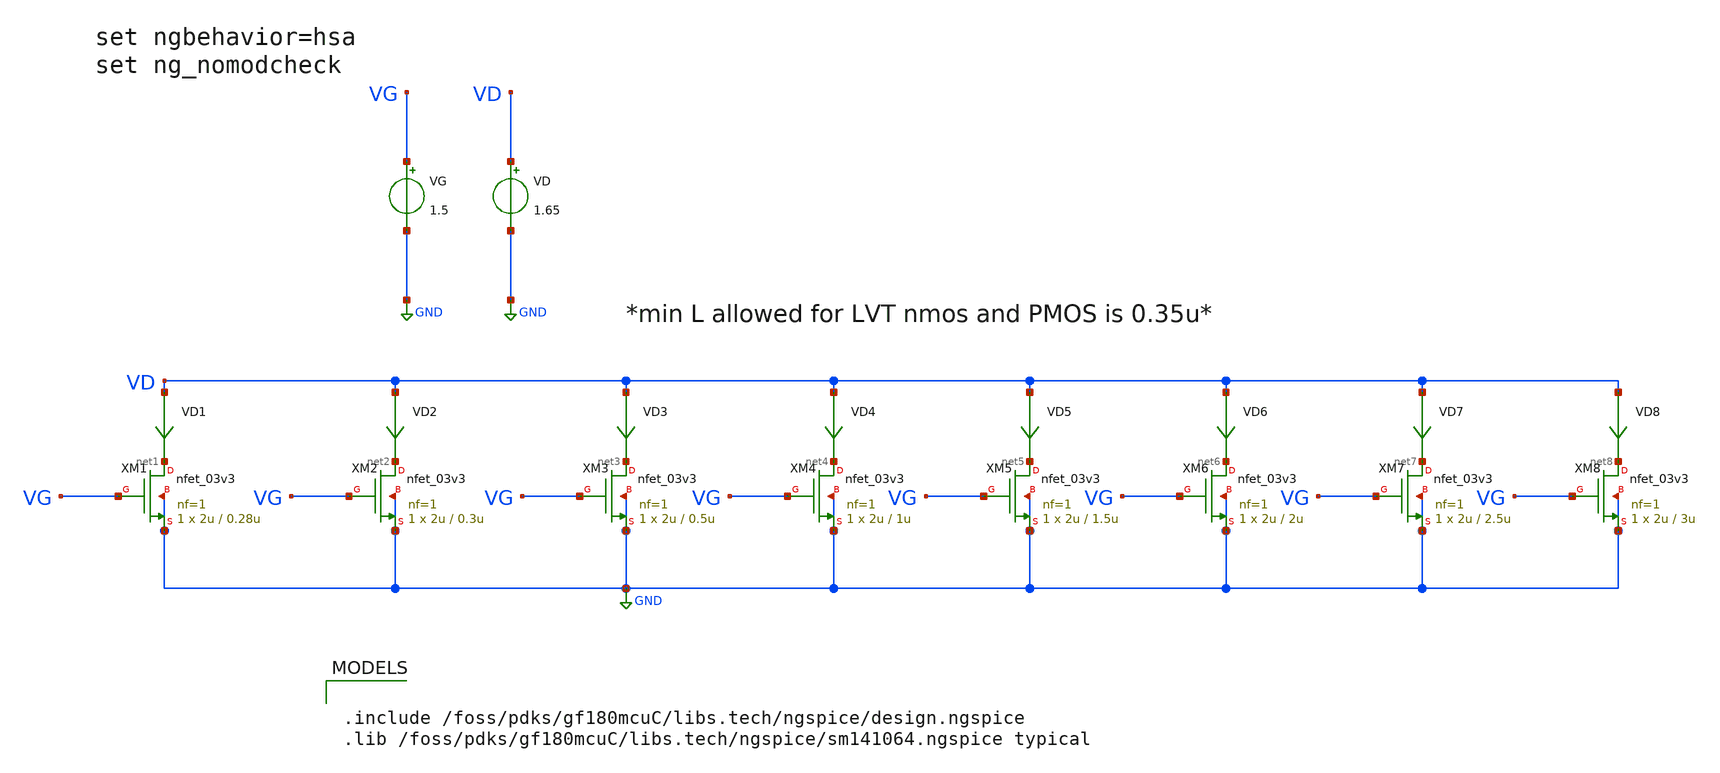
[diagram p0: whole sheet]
** sch_path: Testbench/gmid_nmos_nfet_03v3_tb.sch
**.subckt gmid_nmos_nfet_03v3_tb
VG VG GND 1.5
VD VD GND 1.65
VD1 VD net1 0
.save i(vd1)
VD2 VD net2 0
.save i(vd2)
VD3 VD net3 0
.save i(vd3)
VD4 VD net4 0
.save i(vd4)
VD5 VD net5 0
.save i(vd5)
XM2 net2 VG GND GND nfet_03v3 L=0.3u W=2u nf=1 ad='int((nf+1)/2) * W/nf * 0.18u' as='int((nf+2)/2) * W/nf * 0.18u'
+ pd='2*int((nf+1)/2) * (W/nf + 0.18u)' ps='2*int((nf+2)/2) * (W/nf + 0.18u)' nrd='0.18u / W' nrs='0.18u / W'
+ sa=0 sb=0 sd=0 m=1
XM1 net1 VG GND GND nfet_03v3 L=0.28u W=2u nf=1 ad='int((nf+1)/2) * W/nf * 0.18u' as='int((nf+2)/2) * W/nf * 0.18u'
+ pd='2*int((nf+1)/2) * (W/nf + 0.18u)' ps='2*int((nf+2)/2) * (W/nf + 0.18u)' nrd='0.18u / W' nrs='0.18u / W'
+ sa=0 sb=0 sd=0 m=1
XM3 net3 VG GND GND nfet_03v3 L=0.5u W=2u nf=1 ad='int((nf+1)/2) * W/nf * 0.18u' as='int((nf+2)/2) * W/nf * 0.18u'
+ pd='2*int((nf+1)/2) * (W/nf + 0.18u)' ps='2*int((nf+2)/2) * (W/nf + 0.18u)' nrd='0.18u / W' nrs='0.18u / W'
+ sa=0 sb=0 sd=0 m=1
XM4 net4 VG GND GND nfet_03v3 L=1u W=2u nf=1 ad='int((nf+1)/2) * W/nf * 0.18u' as='int((nf+2)/2) * W/nf * 0.18u'
+ pd='2*int((nf+1)/2) * (W/nf + 0.18u)' ps='2*int((nf+2)/2) * (W/nf + 0.18u)' nrd='0.18u / W' nrs='0.18u / W'
+ sa=0 sb=0 sd=0 m=1
XM5 net5 VG GND GND nfet_03v3 L=1.5u W=2u nf=1 ad='int((nf+1)/2) * W/nf * 0.18u' as='int((nf+2)/2) * W/nf * 0.18u'
+ pd='2*int((nf+1)/2) * (W/nf + 0.18u)' ps='2*int((nf+2)/2) * (W/nf + 0.18u)' nrd='0.18u / W' nrs='0.18u / W'
+ sa=0 sb=0 sd=0 m=1
VD6 VD net6 0
.save i(vd6)
XM6 net6 VG GND GND nfet_03v3 L=2u W=2u nf=1 ad='int((nf+1)/2) * W/nf * 0.18u' as='int((nf+2)/2) * W/nf * 0.18u'
+ pd='2*int((nf+1)/2) * (W/nf + 0.18u)' ps='2*int((nf+2)/2) * (W/nf + 0.18u)' nrd='0.18u / W' nrs='0.18u / W'
+ sa=0 sb=0 sd=0 m=1
VD7 VD net7 0
.save i(vd7)
XM7 net7 VG GND GND nfet_03v3 L=2.5u W=2u nf=1 ad='int((nf+1)/2) * W/nf * 0.18u' as='int((nf+2)/2) * W/nf * 0.18u'
+ pd='2*int((nf+1)/2) * (W/nf + 0.18u)' ps='2*int((nf+2)/2) * (W/nf + 0.18u)' nrd='0.18u / W' nrs='0.18u / W'
+ sa=0 sb=0 sd=0 m=1
VD8 VD net8 0
.save i(vd8)
XM8 net8 VG GND GND nfet_03v3 L=3u W=2u nf=1 ad='int((nf+1)/2) * W/nf * 0.18u' as='int((nf+2)/2) * W/nf * 0.18u'
+ pd='2*int((nf+1)/2) * (W/nf + 0.18u)' ps='2*int((nf+2)/2) * (W/nf + 0.18u)' nrd='0.18u / W' nrs='0.18u / W'
+ sa=0 sb=0 sd=0 m=1
**** begin user architecture code


* ngspice commands
.option wnflag=1
.option savecurrents
.control
save all
save @m.xm1.m0[gm]
save @m.xm2.m0[gm]
save @m.xm3.m0[gm]
save @m.xm4.m0[gm]
save @m.xm5.m0[gm]
save @m.xm6.m0[gm]
save @m.xm7.m0[gm]
save @m.xm8.m0[gm]
save @m.xm1.m0[vth]
save @m.xm2.m0[vth]
save @m.xm3.m0[vth]
save @m.xm4.m0[vth]
save @m.xm5.m0[vth]
save @m.xm6.m0[vth]
save @m.xm7.m0[vth]
save @m.xm8.m0[vth]
save @m.xm1.m0[gds]
save @m.xm2.m0[gds]
save @m.xm3.m0[gds]
save @m.xm4.m0[gds]
save @m.xm5.m0[gds]
save @m.xm6.m0[gds]
save @m.xm7.m0[gds]
save @m.xm8.m0[gds]

dc VG 0.05 3.3 0.05
** remove zero length vectors to prevent write errors
remzerovec
write /foss/designs/gf180mcu-sim/gmid_nmos_tb.raw
plot @m.xm1.m0[gm]
plot @m.xm2.m0[gm]
plot @m.xm3.m0[gm]
plot @m.xm4.m0[gm]
plot @m.xm5.m0[gm]
plot @m.xm6.m0[gm]
plot @m.xm7.m0[gm]
plot @m.xm8.m0[gm]

wrdata gmid_nmos_1_nfet_03v3_tb.txt @m.xm1.m0[gm] i(VD1) @m.xm1.m0[vth] @m.xm1.m0[gds]
wrdata gmid_nmos_2_nfet_03v3_tb.txt @m.xm2.m0[gm] i(VD2) @m.xm2.m0[vth] @m.xm2.m0[gds]
wrdata gmid_nmos_3_nfet_03v3_tb.txt @m.xm3.m0[gm] i(VD3) @m.xm3.m0[vth] @m.xm3.m0[gds]
wrdata gmid_nmos_4_nfet_03v3_tb.txt @m.xm4.m0[gm] i(VD4) @m.xm4.m0[vth] @m.xm4.m0[gds]
wrdata gmid_nmos_5_nfet_03v3_tb.txt @m.xm5.m0[gm] i(VD5) @m.xm5.m0[vth] @m.xm5.m0[gds]
wrdata gmid_nmos_6_nfet_03v3_tb.txt @m.xm6.m0[gm] i(VD6) @m.xm6.m0[vth] @m.xm6.m0[gds]
wrdata gmid_nmos_7_nfet_03v3_tb.txt @m.xm7.m0[gm] i(VD7) @m.xm7.m0[vth] @m.xm7.m0[gds]
wrdata gmid_nmos_8_nfet_03v3_tb.txt @m.xm8.m0[gm] i(VD8) @m.xm8.m0[vth] @m.xm8.m0[gds]

remzerovec
write /foss/designs/gf180mcu-sim/gmid_nmos_tb.raw
quit 0
.endc



.include /foss/pdks/gf180mcuC/libs.tech/ngspice/design.ngspice
.lib /foss/pdks/gf180mcuC/libs.tech/ngspice/sm141064.ngspice typical

**** end user architecture code
**.ends
.GLOBAL GND
.end
